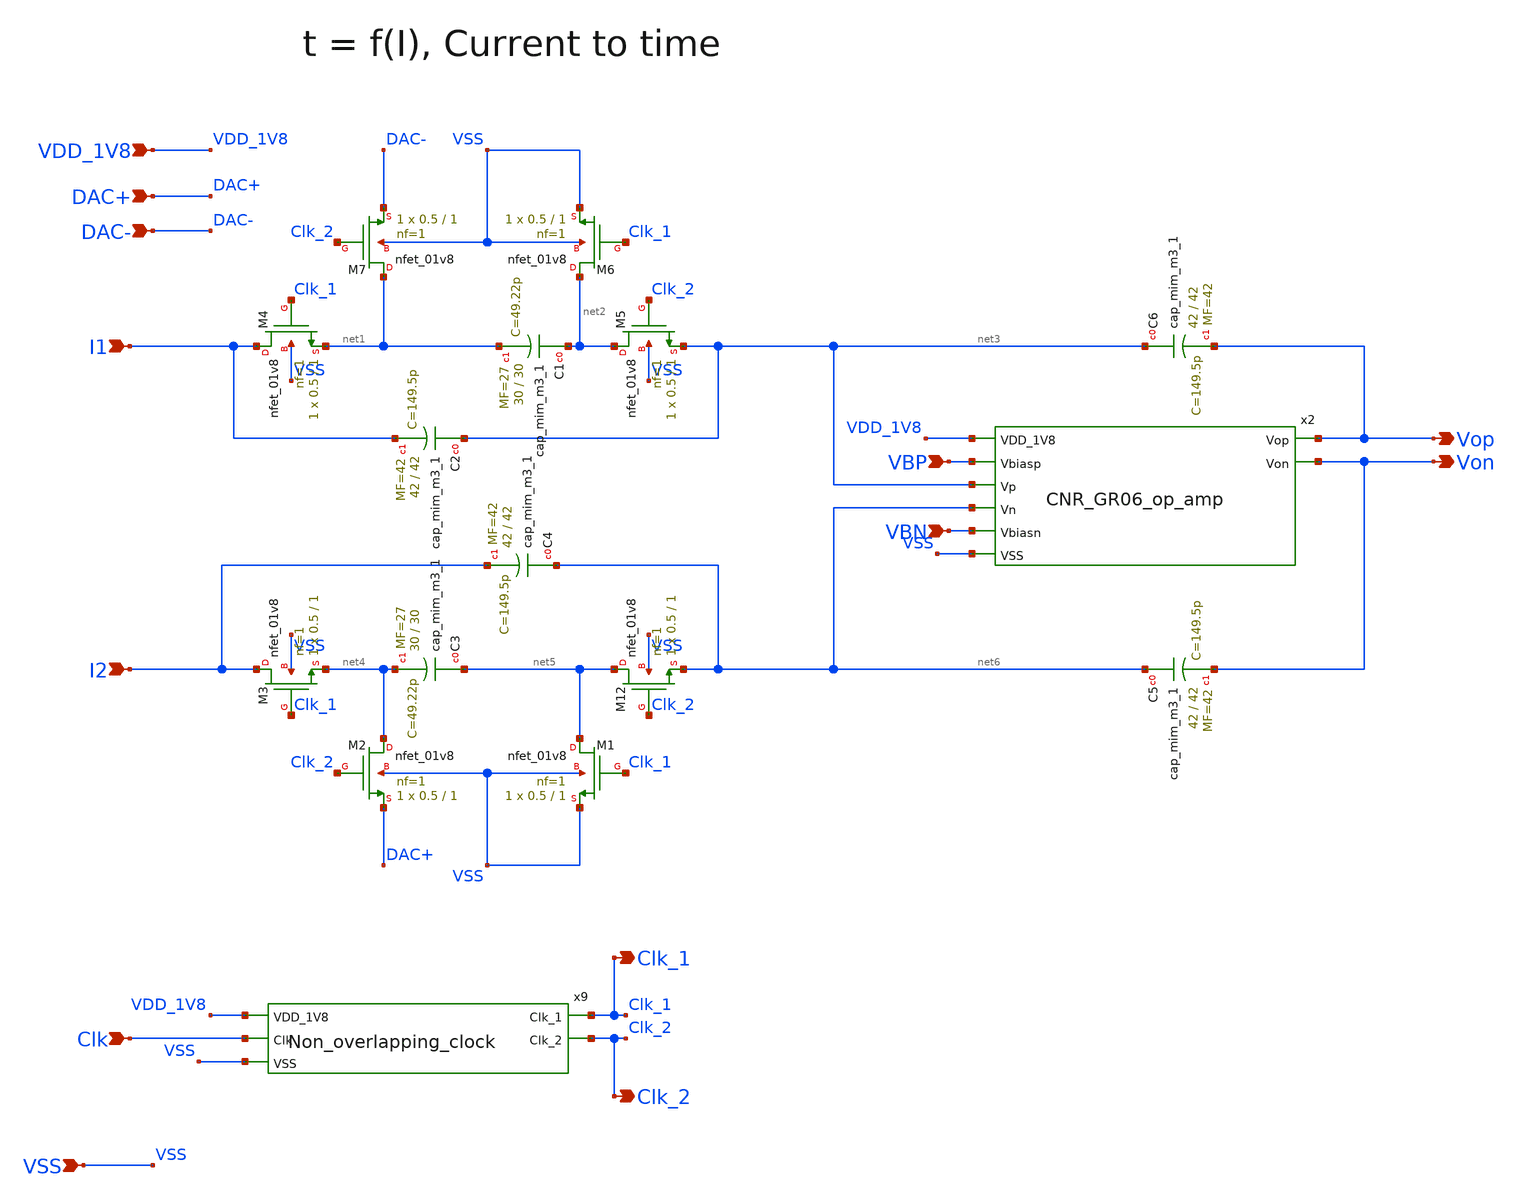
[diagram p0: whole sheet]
** sch_path: design/CNR_GR06_SKY130NM/CNR_GR06_I_to_t.sch
**.subckt CNR_GR06_I_to_t I2 VDD_1V8 VSS I1 Clk Von Vop Clk_1 Clk_2 DAC+ DAC- VBN VBP
*.ipin I2
*.ipin VDD_1V8
*.ipin VSS
*.ipin I1
*.ipin Clk
*.opin Von
*.opin Vop
*.opin Clk_1
*.opin Clk_2
*.ipin DAC+
*.ipin DAC-
*.ipin VBN
*.ipin VBP
XC1 net2 net1 sky130_fd_pr__cap_mim_m3_1 W=30 L=30 MF=27 m=27
XC2 net3 I1 sky130_fd_pr__cap_mim_m3_1 W=42 L=42 MF=42 m=42
XC3 net5 net4 sky130_fd_pr__cap_mim_m3_1 W=30 L=30 MF=27 m=27
XC4 net6 I2 sky130_fd_pr__cap_mim_m3_1 W=42 L=42 MF=42 m=42
XC5 net6 Von sky130_fd_pr__cap_mim_m3_1 W=42 L=42 MF=42 m=42
XC6 net3 Vop sky130_fd_pr__cap_mim_m3_1 W=42 L=42 MF=42 m=42
x9 VDD_1V8 Clk Clk_1 Clk_2 VSS Non_overlapping_clock
x2 VDD_1V8 VBP Vop net3 Von net6 VBN VSS CNR_GR06_op_amp
XM12 net5 Clk_2 net6 VSS sky130_fd_pr__nfet_01v8 L=1 W=0.5 nf=1 ad='int((nf+1)/2) * W/nf * 0.29' as='int((nf+2)/2) * W/nf * 0.29'
+ pd='2*int((nf+1)/2) * (W/nf + 0.29)' ps='2*int((nf+2)/2) * (W/nf + 0.29)' nrd='0.29 / W' nrs='0.29 / W'
+ sa=0 sb=0 sd=0 mult=1 m=1
XM1 net5 Clk_1 VSS VSS sky130_fd_pr__nfet_01v8 L=1 W=0.5 nf=1 ad='int((nf+1)/2) * W/nf * 0.29' as='int((nf+2)/2) * W/nf * 0.29'
+ pd='2*int((nf+1)/2) * (W/nf + 0.29)' ps='2*int((nf+2)/2) * (W/nf + 0.29)' nrd='0.29 / W' nrs='0.29 / W'
+ sa=0 sb=0 sd=0 mult=1 m=1
XM2 net4 Clk_2 DAC+ VSS sky130_fd_pr__nfet_01v8 L=1 W=0.5 nf=1 ad='int((nf+1)/2) * W/nf * 0.29' as='int((nf+2)/2) * W/nf * 0.29'
+ pd='2*int((nf+1)/2) * (W/nf + 0.29)' ps='2*int((nf+2)/2) * (W/nf + 0.29)' nrd='0.29 / W' nrs='0.29 / W'
+ sa=0 sb=0 sd=0 mult=1 m=1
XM3 I2 Clk_1 net4 VSS sky130_fd_pr__nfet_01v8 L=1 W=0.5 nf=1 ad='int((nf+1)/2) * W/nf * 0.29' as='int((nf+2)/2) * W/nf * 0.29'
+ pd='2*int((nf+1)/2) * (W/nf + 0.29)' ps='2*int((nf+2)/2) * (W/nf + 0.29)' nrd='0.29 / W' nrs='0.29 / W'
+ sa=0 sb=0 sd=0 mult=1 m=1
XM4 I1 Clk_1 net1 VSS sky130_fd_pr__nfet_01v8 L=1 W=0.5 nf=1 ad='int((nf+1)/2) * W/nf * 0.29' as='int((nf+2)/2) * W/nf * 0.29'
+ pd='2*int((nf+1)/2) * (W/nf + 0.29)' ps='2*int((nf+2)/2) * (W/nf + 0.29)' nrd='0.29 / W' nrs='0.29 / W'
+ sa=0 sb=0 sd=0 mult=1 m=1
XM5 net2 Clk_2 net3 VSS sky130_fd_pr__nfet_01v8 L=1 W=0.5 nf=1 ad='int((nf+1)/2) * W/nf * 0.29' as='int((nf+2)/2) * W/nf * 0.29'
+ pd='2*int((nf+1)/2) * (W/nf + 0.29)' ps='2*int((nf+2)/2) * (W/nf + 0.29)' nrd='0.29 / W' nrs='0.29 / W'
+ sa=0 sb=0 sd=0 mult=1 m=1
XM6 net2 Clk_1 VSS VSS sky130_fd_pr__nfet_01v8 L=1 W=0.5 nf=1 ad='int((nf+1)/2) * W/nf * 0.29' as='int((nf+2)/2) * W/nf * 0.29'
+ pd='2*int((nf+1)/2) * (W/nf + 0.29)' ps='2*int((nf+2)/2) * (W/nf + 0.29)' nrd='0.29 / W' nrs='0.29 / W'
+ sa=0 sb=0 sd=0 mult=1 m=1
XM7 net1 Clk_2 DAC- VSS sky130_fd_pr__nfet_01v8 L=1 W=0.5 nf=1 ad='int((nf+1)/2) * W/nf * 0.29' as='int((nf+2)/2) * W/nf * 0.29'
+ pd='2*int((nf+1)/2) * (W/nf + 0.29)' ps='2*int((nf+2)/2) * (W/nf + 0.29)' nrd='0.29 / W' nrs='0.29 / W'
+ sa=0 sb=0 sd=0 mult=1 m=1
**.ends
.end
